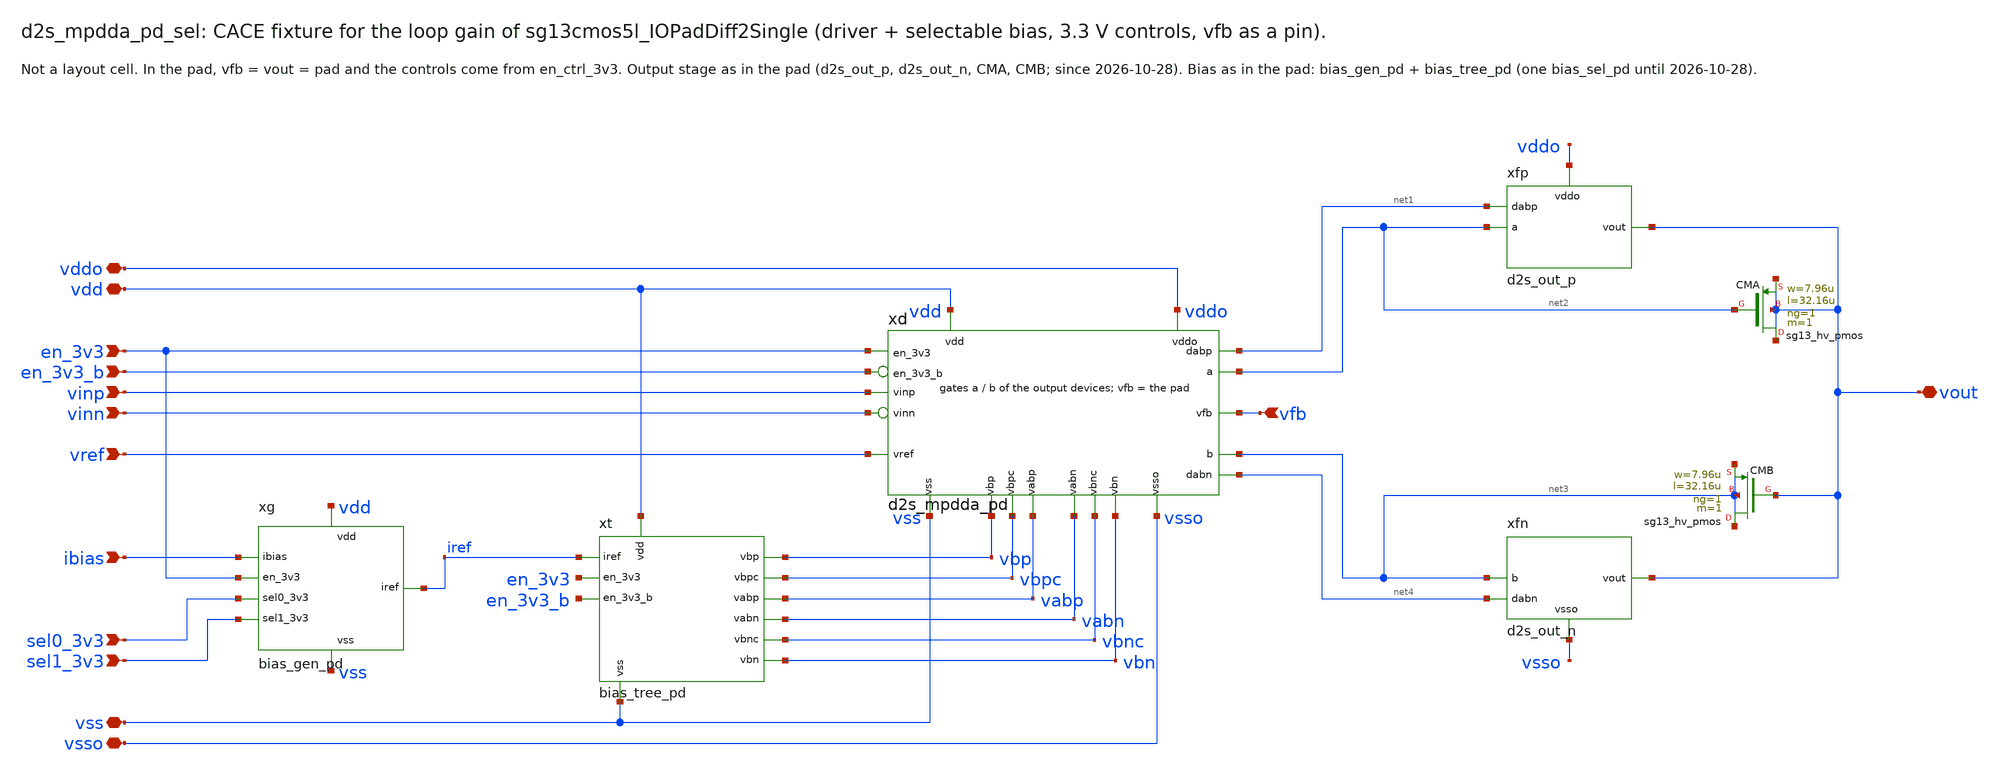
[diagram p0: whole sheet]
** sch_path: macros/sg13cmos5l_IOPadDiff2Single/schematic/xschem/d2s_mpdda_pd_sel.sch
**.subckt d2s_mpdda_pd_sel vdd vss vddo vsso vinp vinn vref ibias en_3v3 sel0_3v3 sel1_3v3 en_3v3_b
*+ vout vfb
*.iopin vdd
*.iopin vss
*.iopin vddo
*.iopin vsso
*.ipin vinp
*.ipin vinn
*.ipin vref
*.ipin ibias
*.ipin en_3v3
*.ipin sel0_3v3
*.ipin sel1_3v3
*.ipin en_3v3_b
*.iopin vout
*.ipin vfb
xd vdd vss vddo vsso vinp vinn vref vfb net2 net3 net1 net4 vbp vbn vbpc vbnc vabp vabn en_3v3
+ en_3v3_b d2s_mpdda_pd
xfp vddo net2 vout net1 d2s_out_p
xfn vsso net3 vout net4 d2s_out_n
XCMA vout net2 vout vout sg13_hv_pmos w=7.96u l=32.16u ng=1 m=1 mm_ok=1
XCMB net3 vout net3 net3 sg13_hv_pmos w=7.96u l=32.16u ng=1 m=1 mm_ok=1
xg vdd vss ibias iref en_3v3 sel0_3v3 sel1_3v3 bias_gen_pd
xt vdd vss iref vbp vbn vbpc vbnc vabp vabn en_3v3 en_3v3_b bias_tree_pd
**.ends
.end
